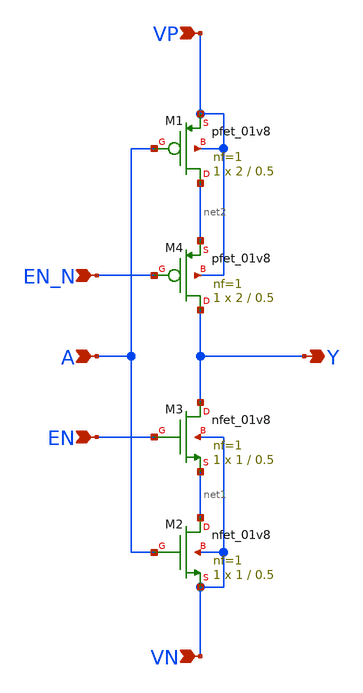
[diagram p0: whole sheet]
** sch_path: ADC/4bit_C2C/MagicAndSpice/EE431_FinalProj/tristate_inv.sch
**.subckt tristate_inv A Y VP VN EN_N EN
*.ipin A
*.opin Y
*.ipin VP
*.ipin VN
*.ipin EN_N
*.ipin EN
XM1 net2 A VP VP sky130_fd_pr__pfet_01v8 L=0.5 W=2 nf=1 ad='int((nf+1)/2) * W/nf * 0.29' as='int((nf+2)/2) * W/nf * 0.29'
+ pd='2*int((nf+1)/2) * (W/nf + 0.29)' ps='2*int((nf+2)/2) * (W/nf + 0.29)' nrd='0.29 / W' nrs='0.29 / W'
+ sa=0 sb=0 sd=0 mult=1 m=1
XM2 net1 A VN VN sky130_fd_pr__nfet_01v8 L=0.5 W=1 nf=1 ad='int((nf+1)/2) * W/nf * 0.29' as='int((nf+2)/2) * W/nf * 0.29'
+ pd='2*int((nf+1)/2) * (W/nf + 0.29)' ps='2*int((nf+2)/2) * (W/nf + 0.29)' nrd='0.29 / W' nrs='0.29 / W'
+ sa=0 sb=0 sd=0 mult=1 m=1
XM3 Y EN net1 VN sky130_fd_pr__nfet_01v8 L=0.5 W=1 nf=1 ad='int((nf+1)/2) * W/nf * 0.29' as='int((nf+2)/2) * W/nf * 0.29'
+ pd='2*int((nf+1)/2) * (W/nf + 0.29)' ps='2*int((nf+2)/2) * (W/nf + 0.29)' nrd='0.29 / W' nrs='0.29 / W'
+ sa=0 sb=0 sd=0 mult=1 m=1
XM4 Y EN_N net2 VP sky130_fd_pr__pfet_01v8 L=0.5 W=2 nf=1 ad='int((nf+1)/2) * W/nf * 0.29' as='int((nf+2)/2) * W/nf * 0.29'
+ pd='2*int((nf+1)/2) * (W/nf + 0.29)' ps='2*int((nf+2)/2) * (W/nf + 0.29)' nrd='0.29 / W' nrs='0.29 / W'
+ sa=0 sb=0 sd=0 mult=1 m=1
**.ends
.end
